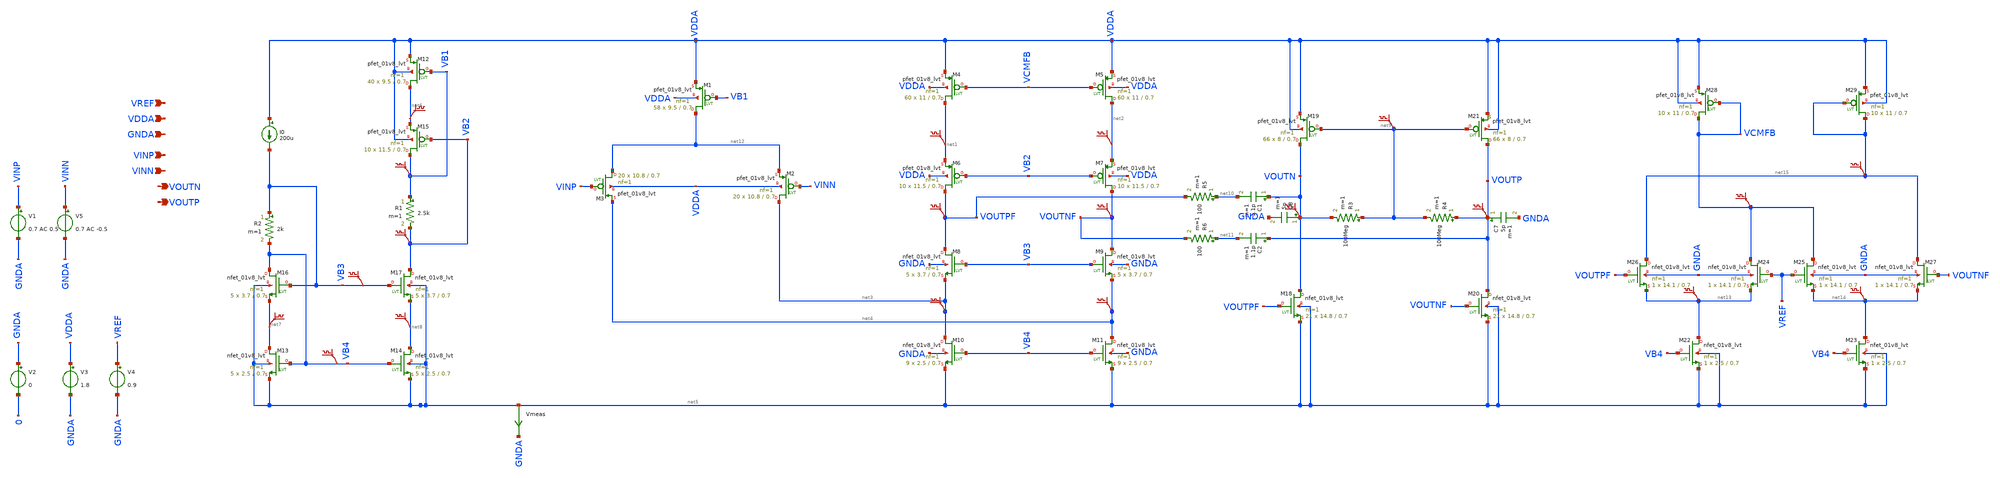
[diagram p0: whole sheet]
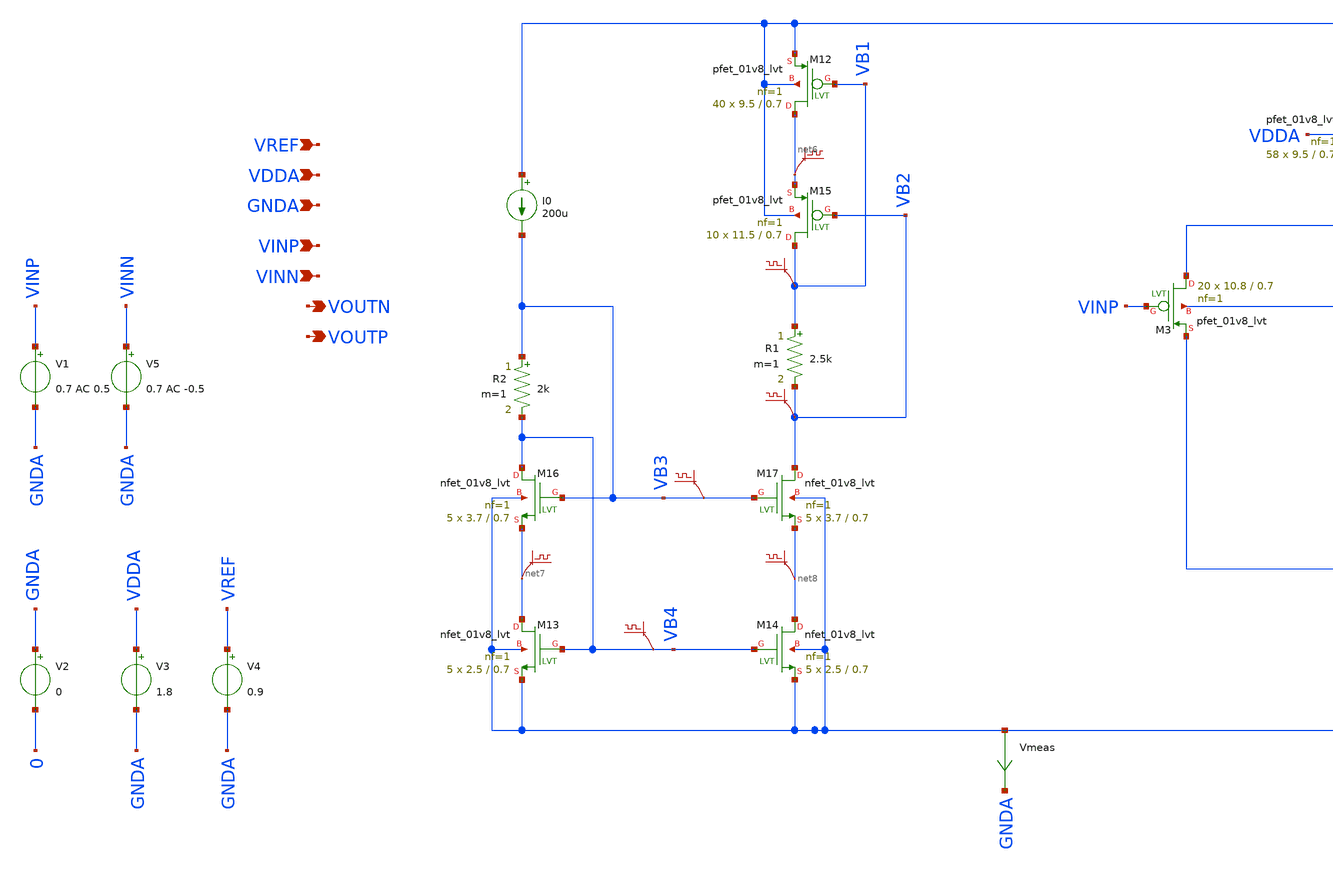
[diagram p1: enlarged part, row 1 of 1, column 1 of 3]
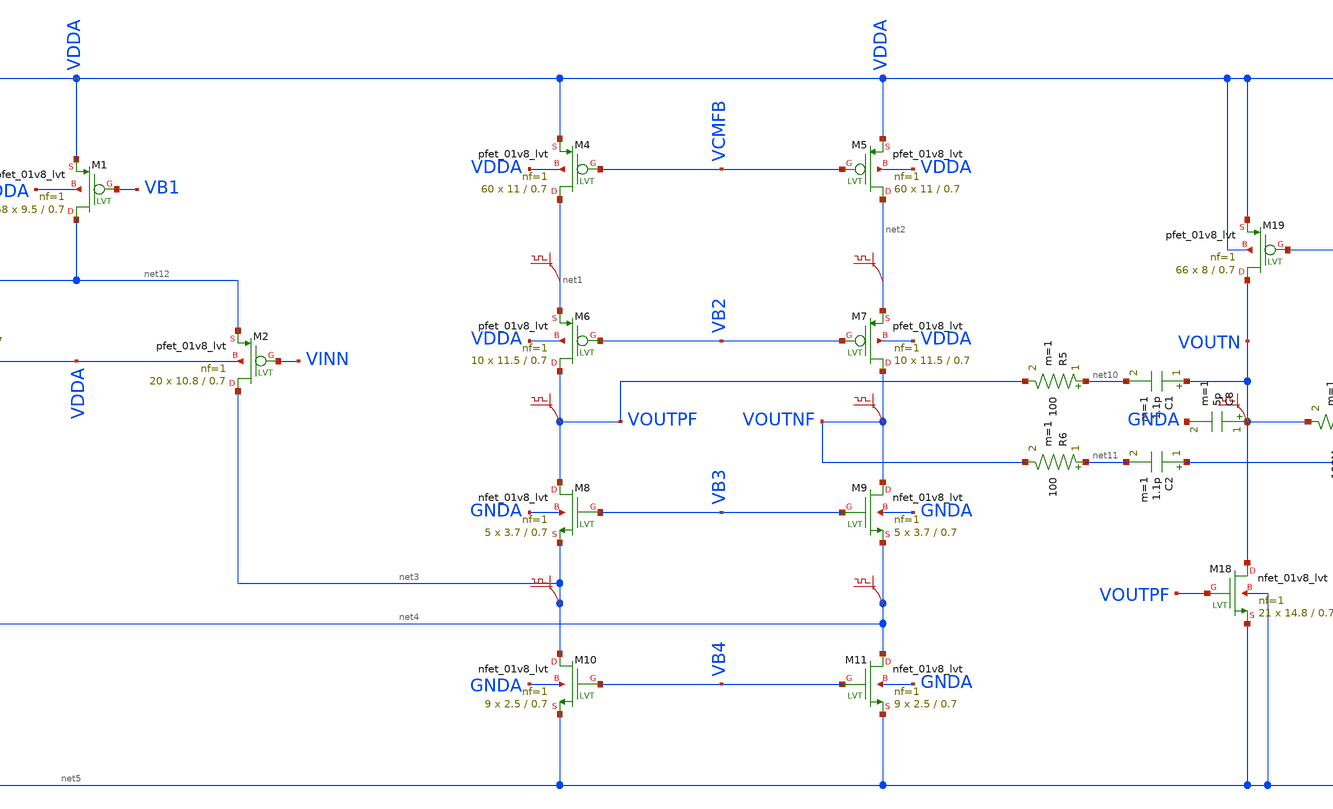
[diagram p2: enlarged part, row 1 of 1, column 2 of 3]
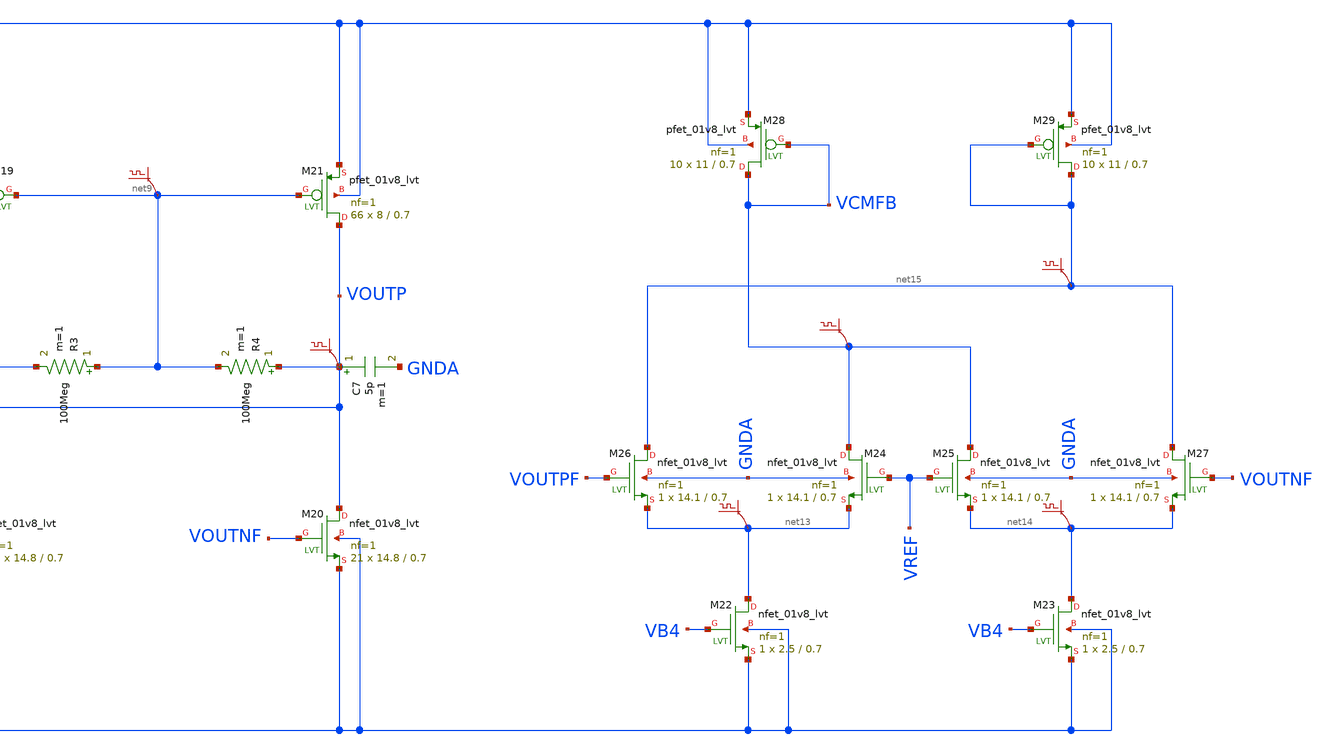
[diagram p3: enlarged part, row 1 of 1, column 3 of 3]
** sch_path: P_in_folded_cascode.sch
**.subckt P_in_folded_cascode VINP VINN VOUTN VOUTP VDDA GNDA VREF
*.ipin VINP
*.ipin VINN
*.opin VOUTN
*.opin VOUTP
*.ipin VDDA
*.ipin GNDA
*.ipin VREF
XM4 net1 VCMFB VDDA VDDA sky130_fd_pr__pfet_01v8_lvt L=0.7 W=11 nf=1 ad='int((nf+1)/2) * W/nf * 0.29'
+ as='int((nf+2)/2) * W/nf * 0.29' pd='2*int((nf+1)/2) * (W/nf + 0.29)' ps='2*int((nf+2)/2) * (W/nf + 0.29)'
+ nrd='0.29 / W' nrs='0.29 / W' sa=0 sb=0 sd=0 mult=60 m=60
XM5 net2 VCMFB VDDA VDDA sky130_fd_pr__pfet_01v8_lvt L=0.7 W=11 nf=1 ad='int((nf+1)/2) * W/nf * 0.29'
+ as='int((nf+2)/2) * W/nf * 0.29' pd='2*int((nf+1)/2) * (W/nf + 0.29)' ps='2*int((nf+2)/2) * (W/nf + 0.29)'
+ nrd='0.29 / W' nrs='0.29 / W' sa=0 sb=0 sd=0 mult=60 m=60
XM6 VOUTPF VB2 net1 VDDA sky130_fd_pr__pfet_01v8_lvt L=0.7 W=11.5 nf=1 ad='int((nf+1)/2) * W/nf * 0.29'
+ as='int((nf+2)/2) * W/nf * 0.29' pd='2*int((nf+1)/2) * (W/nf + 0.29)' ps='2*int((nf+2)/2) * (W/nf + 0.29)'
+ nrd='0.29 / W' nrs='0.29 / W' sa=0 sb=0 sd=0 mult=10 m=10
XM7 VOUTNF VB2 net2 VDDA sky130_fd_pr__pfet_01v8_lvt L=0.7 W=11.5 nf=1 ad='int((nf+1)/2) * W/nf * 0.29'
+ as='int((nf+2)/2) * W/nf * 0.29' pd='2*int((nf+1)/2) * (W/nf + 0.29)' ps='2*int((nf+2)/2) * (W/nf + 0.29)'
+ nrd='0.29 / W' nrs='0.29 / W' sa=0 sb=0 sd=0 mult=10 m=10
XM8 VOUTPF VB3 net3 GNDA sky130_fd_pr__nfet_01v8_lvt L=0.7 W=3.7 nf=1 ad='int((nf+1)/2) * W/nf * 0.29'
+ as='int((nf+2)/2) * W/nf * 0.29' pd='2*int((nf+1)/2) * (W/nf + 0.29)' ps='2*int((nf+2)/2) * (W/nf + 0.29)'
+ nrd='0.29 / W' nrs='0.29 / W' sa=0 sb=0 sd=0 mult=5 m=5
XM9 VOUTNF VB3 net4 GNDA sky130_fd_pr__nfet_01v8_lvt L=0.7 W=3.7 nf=1 ad='int((nf+1)/2) * W/nf * 0.29'
+ as='int((nf+2)/2) * W/nf * 0.29' pd='2*int((nf+1)/2) * (W/nf + 0.29)' ps='2*int((nf+2)/2) * (W/nf + 0.29)'
+ nrd='0.29 / W' nrs='0.29 / W' sa=0 sb=0 sd=0 mult=5 m=5
XM10 net3 VB4 net5 GNDA sky130_fd_pr__nfet_01v8_lvt L=0.7 W=2.5 nf=1 ad='int((nf+1)/2) * W/nf * 0.29'
+ as='int((nf+2)/2) * W/nf * 0.29' pd='2*int((nf+1)/2) * (W/nf + 0.29)' ps='2*int((nf+2)/2) * (W/nf + 0.29)'
+ nrd='0.29 / W' nrs='0.29 / W' sa=0 sb=0 sd=0 mult=9 m=9
XM11 net4 VB4 net5 GNDA sky130_fd_pr__nfet_01v8_lvt L=0.7 W=2.5 nf=1 ad='int((nf+1)/2) * W/nf * 0.29'
+ as='int((nf+2)/2) * W/nf * 0.29' pd='2*int((nf+1)/2) * (W/nf + 0.29)' ps='2*int((nf+2)/2) * (W/nf + 0.29)'
+ nrd='0.29 / W' nrs='0.29 / W' sa=0 sb=0 sd=0 mult=9 m=9
XM12 net6 VB1 VDDA VDDA sky130_fd_pr__pfet_01v8_lvt L=0.7 W=9.5 nf=1 ad='int((nf+1)/2) * W/nf * 0.29'
+ as='int((nf+2)/2) * W/nf * 0.29' pd='2*int((nf+1)/2) * (W/nf + 0.29)' ps='2*int((nf+2)/2) * (W/nf + 0.29)'
+ nrd='0.29 / W' nrs='0.29 / W' sa=0 sb=0 sd=0 mult=40 m=40
XM15 VB1 VB2 net6 VDDA sky130_fd_pr__pfet_01v8_lvt L=0.7 W=11.5 nf=1 ad='int((nf+1)/2) * W/nf * 0.29'
+ as='int((nf+2)/2) * W/nf * 0.29' pd='2*int((nf+1)/2) * (W/nf + 0.29)' ps='2*int((nf+2)/2) * (W/nf + 0.29)'
+ nrd='0.29 / W' nrs='0.29 / W' sa=0 sb=0 sd=0 mult=10 m=10
.save v(vb1)
.save v(net6)
R1 VB1 VB2 2.5k m=1
.save v(vb2)
XM13 net7 VB4 net5 net5 sky130_fd_pr__nfet_01v8_lvt L=0.7 W=2.5 nf=1 ad='int((nf+1)/2) * W/nf * 0.29'
+ as='int((nf+2)/2) * W/nf * 0.29' pd='2*int((nf+1)/2) * (W/nf + 0.29)' ps='2*int((nf+2)/2) * (W/nf + 0.29)'
+ nrd='0.29 / W' nrs='0.29 / W' sa=0 sb=0 sd=0 mult=5 m=5
XM14 net8 VB4 net5 net5 sky130_fd_pr__nfet_01v8_lvt L=0.7 W=2.5 nf=1 ad='int((nf+1)/2) * W/nf * 0.29'
+ as='int((nf+2)/2) * W/nf * 0.29' pd='2*int((nf+1)/2) * (W/nf + 0.29)' ps='2*int((nf+2)/2) * (W/nf + 0.29)'
+ nrd='0.29 / W' nrs='0.29 / W' sa=0 sb=0 sd=0 mult=5 m=5
XM16 VB4 VB3 net7 net5 sky130_fd_pr__nfet_01v8_lvt L=0.7 W=3.7 nf=1 ad='int((nf+1)/2) * W/nf * 0.29'
+ as='int((nf+2)/2) * W/nf * 0.29' pd='2*int((nf+1)/2) * (W/nf + 0.29)' ps='2*int((nf+2)/2) * (W/nf + 0.29)'
+ nrd='0.29 / W' nrs='0.29 / W' sa=0 sb=0 sd=0 mult=5 m=5
XM17 VB2 VB3 net8 net5 sky130_fd_pr__nfet_01v8_lvt L=0.7 W=3.7 nf=1 ad='int((nf+1)/2) * W/nf * 0.29'
+ as='int((nf+2)/2) * W/nf * 0.29' pd='2*int((nf+1)/2) * (W/nf + 0.29)' ps='2*int((nf+2)/2) * (W/nf + 0.29)'
+ nrd='0.29 / W' nrs='0.29 / W' sa=0 sb=0 sd=0 mult=5 m=5
.save v(net7)
.save v(net8)
.save v(vb4)
R2 VB3 VB4 2k m=1
I0 VDDA VB3 200u
XM18 VOUTN VOUTPF net5 net5 sky130_fd_pr__nfet_01v8_lvt L=0.7 W=14.8 nf=1 ad='int((nf+1)/2) * W/nf * 0.29'
+ as='int((nf+2)/2) * W/nf * 0.29' pd='2*int((nf+1)/2) * (W/nf + 0.29)' ps='2*int((nf+2)/2) * (W/nf + 0.29)'
+ nrd='0.29 / W' nrs='0.29 / W' sa=0 sb=0 sd=0 mult=21 m=21
XM19 VOUTN net9 VDDA VDDA sky130_fd_pr__pfet_01v8_lvt L=0.7 W=8 nf=1 ad='int((nf+1)/2) * W/nf * 0.29'
+ as='int((nf+2)/2) * W/nf * 0.29' pd='2*int((nf+1)/2) * (W/nf + 0.29)' ps='2*int((nf+2)/2) * (W/nf + 0.29)'
+ nrd='0.29 / W' nrs='0.29 / W' sa=0 sb=0 sd=0 mult=66 m=66
XM20 VOUTP VOUTNF net5 net5 sky130_fd_pr__nfet_01v8_lvt L=0.7 W=14.8 nf=1 ad='int((nf+1)/2) * W/nf * 0.29'
+ as='int((nf+2)/2) * W/nf * 0.29' pd='2*int((nf+1)/2) * (W/nf + 0.29)' ps='2*int((nf+2)/2) * (W/nf + 0.29)'
+ nrd='0.29 / W' nrs='0.29 / W' sa=0 sb=0 sd=0 mult=21 m=21
XM21 VOUTP net9 VDDA VDDA sky130_fd_pr__pfet_01v8_lvt L=0.7 W=8 nf=1 ad='int((nf+1)/2) * W/nf * 0.29'
+ as='int((nf+2)/2) * W/nf * 0.29' pd='2*int((nf+1)/2) * (W/nf + 0.29)' ps='2*int((nf+2)/2) * (W/nf + 0.29)'
+ nrd='0.29 / W' nrs='0.29 / W' sa=0 sb=0 sd=0 mult=66 m=66
R5 net10 VOUTPF 100 m=1
R6 net11 VOUTNF 100 m=1
C1 VOUTN net10 1.1p m=1
C2 VOUTP net11 1.1p m=1
V2 GNDA 0 0
V3 VDDA GNDA 1.8
V4 VREF GNDA 0.9
.save v(net1)
.save v(net2)
.save v(voutpf)
.save v(voutnf)
.save v(net3)
.save v(net4)
.save v(voutn)
.save v(voutp)
.save v(vb3)
XM1 net12 VB1 VDDA VDDA sky130_fd_pr__pfet_01v8_lvt L=0.7 W=9.5 nf=1 ad='int((nf+1)/2) * W/nf * 0.29'
+ as='int((nf+2)/2) * W/nf * 0.29' pd='2*int((nf+1)/2) * (W/nf + 0.29)' ps='2*int((nf+2)/2) * (W/nf + 0.29)'
+ nrd='0.29 / W' nrs='0.29 / W' sa=0 sb=0 sd=0 mult=58 m=58
XM2 net3 VINN net12 VDDA sky130_fd_pr__pfet_01v8_lvt L=0.7 W=10.8 nf=1 ad='int((nf+1)/2) * W/nf * 0.29'
+ as='int((nf+2)/2) * W/nf * 0.29' pd='2*int((nf+1)/2) * (W/nf + 0.29)' ps='2*int((nf+2)/2) * (W/nf + 0.29)'
+ nrd='0.29 / W' nrs='0.29 / W' sa=0 sb=0 sd=0 mult=20 m=20
XM3 net12 VINP net4 VDDA sky130_fd_pr__pfet_01v8_lvt L=0.7 W=10.8 nf=1 ad='int((nf+1)/2) * W/nf * 0.29'
+ as='int((nf+2)/2) * W/nf * 0.29' pd='2*int((nf+1)/2) * (W/nf + 0.29)' ps='2*int((nf+2)/2) * (W/nf + 0.29)'
+ nrd='0.29 / W' nrs='0.29 / W' sa=0 sb=0 sd=0 mult=20 m=20
R3 net9 VOUTN 100Meg m=1
R4 VOUTP net9 100Meg m=1
XM22 net13 VB4 net5 net5 sky130_fd_pr__nfet_01v8_lvt L=0.7 W=2.5 nf=1 ad='int((nf+1)/2) * W/nf * 0.29'
+ as='int((nf+2)/2) * W/nf * 0.29' pd='2*int((nf+1)/2) * (W/nf + 0.29)' ps='2*int((nf+2)/2) * (W/nf + 0.29)'
+ nrd='0.29 / W' nrs='0.29 / W' sa=0 sb=0 sd=0 mult=1 m=1
XM23 net14 VB4 net5 net5 sky130_fd_pr__nfet_01v8_lvt L=0.7 W=2.5 nf=1 ad='int((nf+1)/2) * W/nf * 0.29'
+ as='int((nf+2)/2) * W/nf * 0.29' pd='2*int((nf+1)/2) * (W/nf + 0.29)' ps='2*int((nf+2)/2) * (W/nf + 0.29)'
+ nrd='0.29 / W' nrs='0.29 / W' sa=0 sb=0 sd=0 mult=1 m=1
XM24 VCMFB VREF net13 GNDA sky130_fd_pr__nfet_01v8_lvt L=0.7 W=14.1 nf=1 ad='int((nf+1)/2) * W/nf * 0.29'
+ as='int((nf+2)/2) * W/nf * 0.29' pd='2*int((nf+1)/2) * (W/nf + 0.29)' ps='2*int((nf+2)/2) * (W/nf + 0.29)'
+ nrd='0.29 / W' nrs='0.29 / W' sa=0 sb=0 sd=0 mult=1 m=1
XM25 VCMFB VREF net14 GNDA sky130_fd_pr__nfet_01v8_lvt L=0.7 W=14.1 nf=1 ad='int((nf+1)/2) * W/nf * 0.29'
+ as='int((nf+2)/2) * W/nf * 0.29' pd='2*int((nf+1)/2) * (W/nf + 0.29)' ps='2*int((nf+2)/2) * (W/nf + 0.29)'
+ nrd='0.29 / W' nrs='0.29 / W' sa=0 sb=0 sd=0 mult=1 m=1
XM26 net15 VOUTPF net13 GNDA sky130_fd_pr__nfet_01v8_lvt L=0.7 W=14.1 nf=1 ad='int((nf+1)/2) * W/nf * 0.29'
+ as='int((nf+2)/2) * W/nf * 0.29' pd='2*int((nf+1)/2) * (W/nf + 0.29)' ps='2*int((nf+2)/2) * (W/nf + 0.29)'
+ nrd='0.29 / W' nrs='0.29 / W' sa=0 sb=0 sd=0 mult=1 m=1
XM27 net15 VOUTNF net14 GNDA sky130_fd_pr__nfet_01v8_lvt L=0.7 W=14.1 nf=1 ad='int((nf+1)/2) * W/nf * 0.29'
+ as='int((nf+2)/2) * W/nf * 0.29' pd='2*int((nf+1)/2) * (W/nf + 0.29)' ps='2*int((nf+2)/2) * (W/nf + 0.29)'
+ nrd='0.29 / W' nrs='0.29 / W' sa=0 sb=0 sd=0 mult=1 m=1
XM28 VCMFB VCMFB VDDA VDDA sky130_fd_pr__pfet_01v8_lvt L=0.7 W=11 nf=1 ad='int((nf+1)/2) * W/nf * 0.29'
+ as='int((nf+2)/2) * W/nf * 0.29' pd='2*int((nf+1)/2) * (W/nf + 0.29)' ps='2*int((nf+2)/2) * (W/nf + 0.29)'
+ nrd='0.29 / W' nrs='0.29 / W' sa=0 sb=0 sd=0 mult=10 m=10
XM29 net15 net15 VDDA VDDA sky130_fd_pr__pfet_01v8_lvt L=0.7 W=11 nf=1 ad='int((nf+1)/2) * W/nf * 0.29'
+ as='int((nf+2)/2) * W/nf * 0.29' pd='2*int((nf+1)/2) * (W/nf + 0.29)' ps='2*int((nf+2)/2) * (W/nf + 0.29)'
+ nrd='0.29 / W' nrs='0.29 / W' sa=0 sb=0 sd=0 mult=10 m=10
.save v(net13)
.save v(net14)
.save v(vcmfb)
.save v(net15)
.save v(net9)
C7 VOUTP GNDA 5p m=1
C8 VOUTN GNDA 5p m=1
Vmeas net5 GNDA 0
.save i(vmeas)
V1 VINP GNDA 0.7 AC 0.5
V5 VINN GNDA 0.7 AC -0.5
**** begin user architecture code

** opencircuitdesign pdks install
.lib $::SKYWATER_MODELS/sky130.lib.spice ss



.control
save all
save @m.xm1.msky130_fd_pr__pfet_01v8_lvt[vth]
save @m.xm1.msky130_fd_pr__pfet_01v8_lvt[id]
save @m.xm1.msky130_fd_pr__pfet_01v8_lvt[gds]
save @m.xm1.msky130_fd_pr__pfet_01v8_lvt[gm]
save @m.xm1.msky130_fd_pr__pfet_01v8_lvt[vdsat]
save @m.xm1.msky130_fd_pr__pfet_01v8_lvt[cgg]
save @m.xm1.msky130_fd_pr__pfet_01v8_lvt[cgd]

save @m.xm3.msky130_fd_pr__pfet_01v8_lvt[vth]
save @m.xm3.msky130_fd_pr__pfet_01v8_lvt[id]
save @m.xm3.msky130_fd_pr__pfet_01v8_lvt[gds]
save @m.xm3.msky130_fd_pr__pfet_01v8_lvt[gm]
save @m.xm3.msky130_fd_pr__pfet_01v8_lvt[vdsat]
save @m.xm3.msky130_fd_pr__pfet_01v8_lvt[cgg]
save @m.xm3.msky130_fd_pr__pfet_01v8_lvt[cgd]

save @m.xm8.msky130_fd_pr__nfet_01v8_lvt[vth]
save @m.xm8.msky130_fd_pr__nfet_01v8_lvt[id]
save @m.xm8.msky130_fd_pr__nfet_01v8_lvt[gds]
save @m.xm8.msky130_fd_pr__nfet_01v8_lvt[gm]
save @m.xm8.msky130_fd_pr__nfet_01v8_lvt[vdsat]
save @m.xm8.msky130_fd_pr__nfet_01v8_lvt[cgg]
save @m.xm8.msky130_fd_pr__nfet_01v8_lvt[cgd]

save @m.xm9.msky130_fd_pr__nfet_01v8_lvt[vth]
save @m.xm9.msky130_fd_pr__nfet_01v8_lvt[id]
save @m.xm9.msky130_fd_pr__nfet_01v8_lvt[gds]
save @m.xm9.msky130_fd_pr__nfet_01v8_lvt[gm]
save @m.xm9.msky130_fd_pr__nfet_01v8_lvt[vdsat]
save @m.xm9.msky130_fd_pr__nfet_01v8_lvt[cgg]
save @m.xm9.msky130_fd_pr__nfet_01v8_lvt[cgd]

save @m.xm10.msky130_fd_pr__nfet_01v8_lvt[vth]
save @m.xm10.msky130_fd_pr__nfet_01v8_lvt[id]
save @m.xm10.msky130_fd_pr__nfet_01v8_lvt[gds]
save @m.xm10.msky130_fd_pr__nfet_01v8_lvt[gm]
save @m.xm10.msky130_fd_pr__nfet_01v8_lvt[vdsat]
save @m.xm10.msky130_fd_pr__nfet_01v8_lvt[cgg]
save @m.xm10.msky130_fd_pr__nfet_01v8_lvt[cgd]

save @m.xm11.msky130_fd_pr__nfet_01v8_lvt[vth]
save @m.xm11.msky130_fd_pr__nfet_01v8_lvt[id]
save @m.xm11.msky130_fd_pr__nfet_01v8_lvt[gds]
save @m.xm11.msky130_fd_pr__nfet_01v8_lvt[gm]
save @m.xm11.msky130_fd_pr__nfet_01v8_lvt[vdsat]
save @m.xm11.msky130_fd_pr__nfet_01v8_lvt[cgg]
save @m.xm11.msky130_fd_pr__nfet_01v8_lvt[cgd]

save @m.xm13.msky130_fd_pr__nfet_01v8_lvt[vth]
save @m.xm13.msky130_fd_pr__nfet_01v8_lvt[id]
save @m.xm13.msky130_fd_pr__nfet_01v8_lvt[gds]
save @m.xm13.msky130_fd_pr__nfet_01v8_lvt[gm]
save @m.xm13.msky130_fd_pr__nfet_01v8_lvt[vdsat]
save @m.xm13.msky130_fd_pr__nfet_01v8_lvt[cgg]
save @m.xm13.msky130_fd_pr__nfet_01v8_lvt[cgd]

save @m.xm14.msky130_fd_pr__nfet_01v8_lvt[vth]
save @m.xm14.msky130_fd_pr__nfet_01v8_lvt[id]
save @m.xm14.msky130_fd_pr__nfet_01v8_lvt[gds]
save @m.xm14.msky130_fd_pr__nfet_01v8_lvt[gm]
save @m.xm14.msky130_fd_pr__nfet_01v8_lvt[vdsat]
save @m.xm14.msky130_fd_pr__nfet_01v8_lvt[cgg]
save @m.xm14.msky130_fd_pr__nfet_01v8_lvt[cgd]

save @m.xm16.msky130_fd_pr__nfet_01v8_lvt[vth]
save @m.xm16.msky130_fd_pr__nfet_01v8_lvt[id]
save @m.xm16.msky130_fd_pr__nfet_01v8_lvt[gds]
save @m.xm16.msky130_fd_pr__nfet_01v8_lvt[gm]
save @m.xm16.msky130_fd_pr__nfet_01v8_lvt[vdsat]
save @m.xm16.msky130_fd_pr__nfet_01v8_lvt[cgg]
save @m.xm16.msky130_fd_pr__nfet_01v8_lvt[cgd]

save @m.xm17.msky130_fd_pr__nfet_01v8_lvt[vth]
save @m.xm17.msky130_fd_pr__nfet_01v8_lvt[id]
save @m.xm17.msky130_fd_pr__nfet_01v8_lvt[gds]
save @m.xm17.msky130_fd_pr__nfet_01v8_lvt[gm]
save @m.xm17.msky130_fd_pr__nfet_01v8_lvt[vdsat]
save @m.xm17.msky130_fd_pr__nfet_01v8_lvt[cgg]
save @m.xm17.msky130_fd_pr__nfet_01v8_lvt[cgd]

save @m.xm18.msky130_fd_pr__nfet_01v8_lvt[vth]
save @m.xm18.msky130_fd_pr__nfet_01v8_lvt[id]
save @m.xm18.msky130_fd_pr__nfet_01v8_lvt[gds]
save @m.xm18.msky130_fd_pr__nfet_01v8_lvt[gm]
save @m.xm18.msky130_fd_pr__nfet_01v8_lvt[vdsat]
save @m.xm18.msky130_fd_pr__nfet_01v8_lvt[cgg]
save @m.xm18.msky130_fd_pr__nfet_01v8_lvt[cgd]

save @m.xm20.msky130_fd_pr__nfet_01v8_lvt[vth]
save @m.xm20.msky130_fd_pr__nfet_01v8_lvt[id]
save @m.xm20.msky130_fd_pr__nfet_01v8_lvt[gds]
save @m.xm20.msky130_fd_pr__nfet_01v8_lvt[gm]
save @m.xm20.msky130_fd_pr__nfet_01v8_lvt[vdsat]
save @m.xm20.msky130_fd_pr__nfet_01v8_lvt[cgg]
save @m.xm20.msky130_fd_pr__nfet_01v8_lvt[cgd]

save @m.xm22.msky130_fd_pr__nfet_01v8_lvt[vth]
save @m.xm22.msky130_fd_pr__nfet_01v8_lvt[id]
save @m.xm22.msky130_fd_pr__nfet_01v8_lvt[gds]
save @m.xm22.msky130_fd_pr__nfet_01v8_lvt[gm]
save @m.xm22.msky130_fd_pr__nfet_01v8_lvt[vdsat]
save @m.xm22.msky130_fd_pr__nfet_01v8_lvt[cgg]
save @m.xm22.msky130_fd_pr__nfet_01v8_lvt[cgd]

save @m.xm26.msky130_fd_pr__nfet_01v8_lvt[vth]
save @m.xm26.msky130_fd_pr__nfet_01v8_lvt[id]
save @m.xm26.msky130_fd_pr__nfet_01v8_lvt[gds]
save @m.xm26.msky130_fd_pr__nfet_01v8_lvt[gm]
save @m.xm26.msky130_fd_pr__nfet_01v8_lvt[vdsat]
save @m.xm26.msky130_fd_pr__nfet_01v8_lvt[cgg]
save @m.xm26.msky130_fd_pr__nfet_01v8_lvt[cgd]

save @m.xm25.msky130_fd_pr__nfet_01v8_lvt[vth]
save @m.xm25.msky130_fd_pr__nfet_01v8_lvt[id]
save @m.xm25.msky130_fd_pr__nfet_01v8_lvt[gds]
save @m.xm25.msky130_fd_pr__nfet_01v8_lvt[gm]
save @m.xm25.msky130_fd_pr__nfet_01v8_lvt[vdsat]
save @m.xm25.msky130_fd_pr__nfet_01v8_lvt[cgg]
save @m.xm25.msky130_fd_pr__nfet_01v8_lvt[cgd]

save @m.xm28.msky130_fd_pr__pfet_01v8_lvt[vth]
save @m.xm28.msky130_fd_pr__pfet_01v8_lvt[id]
save @m.xm28.msky130_fd_pr__pfet_01v8_lvt[gds]
save @m.xm28.msky130_fd_pr__pfet_01v8_lvt[gm]
save @m.xm28.msky130_fd_pr__pfet_01v8_lvt[vdsat]
save @m.xm28.msky130_fd_pr__pfet_01v8_lvt[cgg]
save @m.xm28.msky130_fd_pr__pfet_01v8_lvt[cgd]

save @m.xm4.msky130_fd_pr__pfet_01v8_lvt[vth]
save @m.xm4.msky130_fd_pr__pfet_01v8_lvt[id]
save @m.xm4.msky130_fd_pr__pfet_01v8_lvt[gds]
save @m.xm4.msky130_fd_pr__pfet_01v8_lvt[gm]
save @m.xm4.msky130_fd_pr__pfet_01v8_lvt[vdsat]
save @m.xm4.msky130_fd_pr__pfet_01v8_lvt[cgg]
save @m.xm4.msky130_fd_pr__pfet_01v8_lvt[cgd]

save @m.xm5.msky130_fd_pr__pfet_01v8_lvt[vth]
save @m.xm5.msky130_fd_pr__pfet_01v8_lvt[id]
save @m.xm5.msky130_fd_pr__pfet_01v8_lvt[gds]
save @m.xm5.msky130_fd_pr__pfet_01v8_lvt[gm]
save @m.xm5.msky130_fd_pr__pfet_01v8_lvt[vdsat]
save @m.xm5.msky130_fd_pr__pfet_01v8_lvt[cgg]
save @m.xm5.msky130_fd_pr__pfet_01v8_lvt[cgd]

save @m.xm6.msky130_fd_pr__pfet_01v8_lvt[vth]
save @m.xm6.msky130_fd_pr__pfet_01v8_lvt[id]
save @m.xm6.msky130_fd_pr__pfet_01v8_lvt[gds]
save @m.xm6.msky130_fd_pr__pfet_01v8_lvt[gm]
save @m.xm6.msky130_fd_pr__pfet_01v8_lvt[vdsat]
save @m.xm6.msky130_fd_pr__pfet_01v8_lvt[cgg]
save @m.xm6.msky130_fd_pr__pfet_01v8_lvt[cgd]

save @m.xm7.msky130_fd_pr__pfet_01v8_lvt[vth]
save @m.xm7.msky130_fd_pr__pfet_01v8_lvt[id]
save @m.xm7.msky130_fd_pr__pfet_01v8_lvt[gds]
save @m.xm7.msky130_fd_pr__pfet_01v8_lvt[gm]
save @m.xm7.msky130_fd_pr__pfet_01v8_lvt[vdsat]
save @m.xm7.msky130_fd_pr__pfet_01v8_lvt[cgg]
save @m.xm7.msky130_fd_pr__pfet_01v8_lvt[cgd]

save @m.xm12.msky130_fd_pr__pfet_01v8_lvt[vth]
save @m.xm12.msky130_fd_pr__pfet_01v8_lvt[id]
save @m.xm12.msky130_fd_pr__pfet_01v8_lvt[gds]
save @m.xm12.msky130_fd_pr__pfet_01v8_lvt[gm]
save @m.xm12.msky130_fd_pr__pfet_01v8_lvt[vdsat]
save @m.xm12.msky130_fd_pr__pfet_01v8_lvt[cgg]
save @m.xm12.msky130_fd_pr__pfet_01v8_lvt[cgd]

save @m.xm15.msky130_fd_pr__pfet_01v8_lvt[vth]
save @m.xm15.msky130_fd_pr__pfet_01v8_lvt[id]
save @m.xm15.msky130_fd_pr__pfet_01v8_lvt[gds]
save @m.xm15.msky130_fd_pr__pfet_01v8_lvt[gm]
save @m.xm15.msky130_fd_pr__pfet_01v8_lvt[vdsat]
save @m.xm15.msky130_fd_pr__pfet_01v8_lvt[cgg]
save @m.xm15.msky130_fd_pr__pfet_01v8_lvt[cgd]

save @m.xm19.msky130_fd_pr__pfet_01v8_lvt[vth]
save @m.xm19.msky130_fd_pr__pfet_01v8_lvt[id]
save @m.xm19.msky130_fd_pr__pfet_01v8_lvt[gds]
save @m.xm19.msky130_fd_pr__pfet_01v8_lvt[gm]
save @m.xm19.msky130_fd_pr__pfet_01v8_lvt[vdsat]
save @m.xm19.msky130_fd_pr__pfet_01v8_lvt[cgg]
save @m.xm19.msky130_fd_pr__pfet_01v8_lvt[cgd]

save @m.xm21.msky130_fd_pr__pfet_01v8_lvt[vth]
save @m.xm21.msky130_fd_pr__pfet_01v8_lvt[id]
save @m.xm21.msky130_fd_pr__pfet_01v8_lvt[gds]
save @m.xm21.msky130_fd_pr__pfet_01v8_lvt[gm]
save @m.xm21.msky130_fd_pr__pfet_01v8_lvt[vdsat]
save @m.xm21.msky130_fd_pr__pfet_01v8_lvt[cgg]
save @m.xm21.msky130_fd_pr__pfet_01v8_lvt[cgd]

*tran 1n 2u
*op
ac dec 100 1 100T
*setplot new
*let frequency = ac.frequency
let T = ac.voutp-ac.voutn
let T_mag = db(T)
let T_ph  = cph(T)*180/pi

*let T1 = ac.voutpc
*let PSRR = T/T1
*let PSRR_mag = db(PSRR)
*let PSRR_ph  = cph(PSRR)*180/pi
*let T1_mag = db(T1)
let T1_ph  = cph(T1)*180/pi
*let T2 = (ac.outp-ac.outn)/(ac.outp1-ac.outn1)
*let T2_mag = db(T2)
*let T2_ph  = cph(T2)*180/pi
plot T_mag T_ph xlog
*plot T1_mag T1_ph xlog
*plot PSRR_mag PSRR_ph xlog
write P_in_folded_cascode.raw
.endc

**** end user architecture code
**.ends
.end
